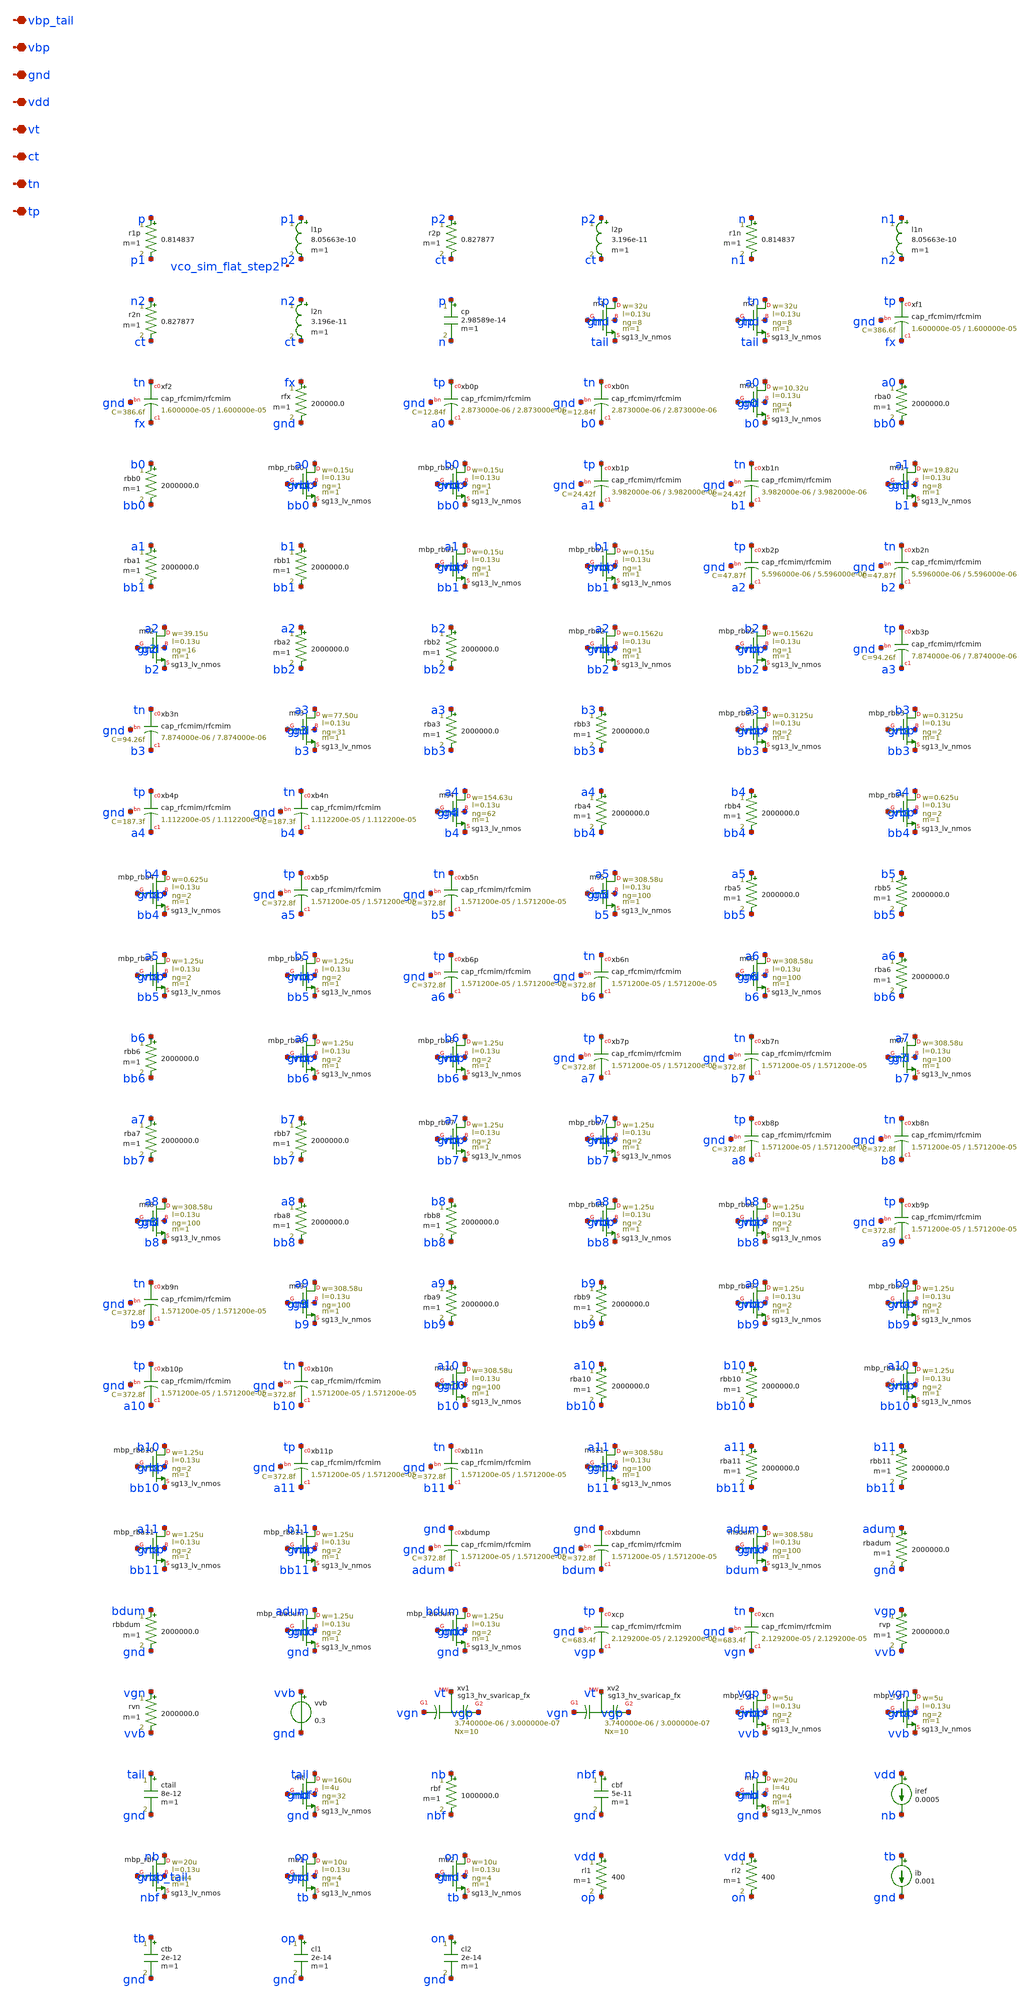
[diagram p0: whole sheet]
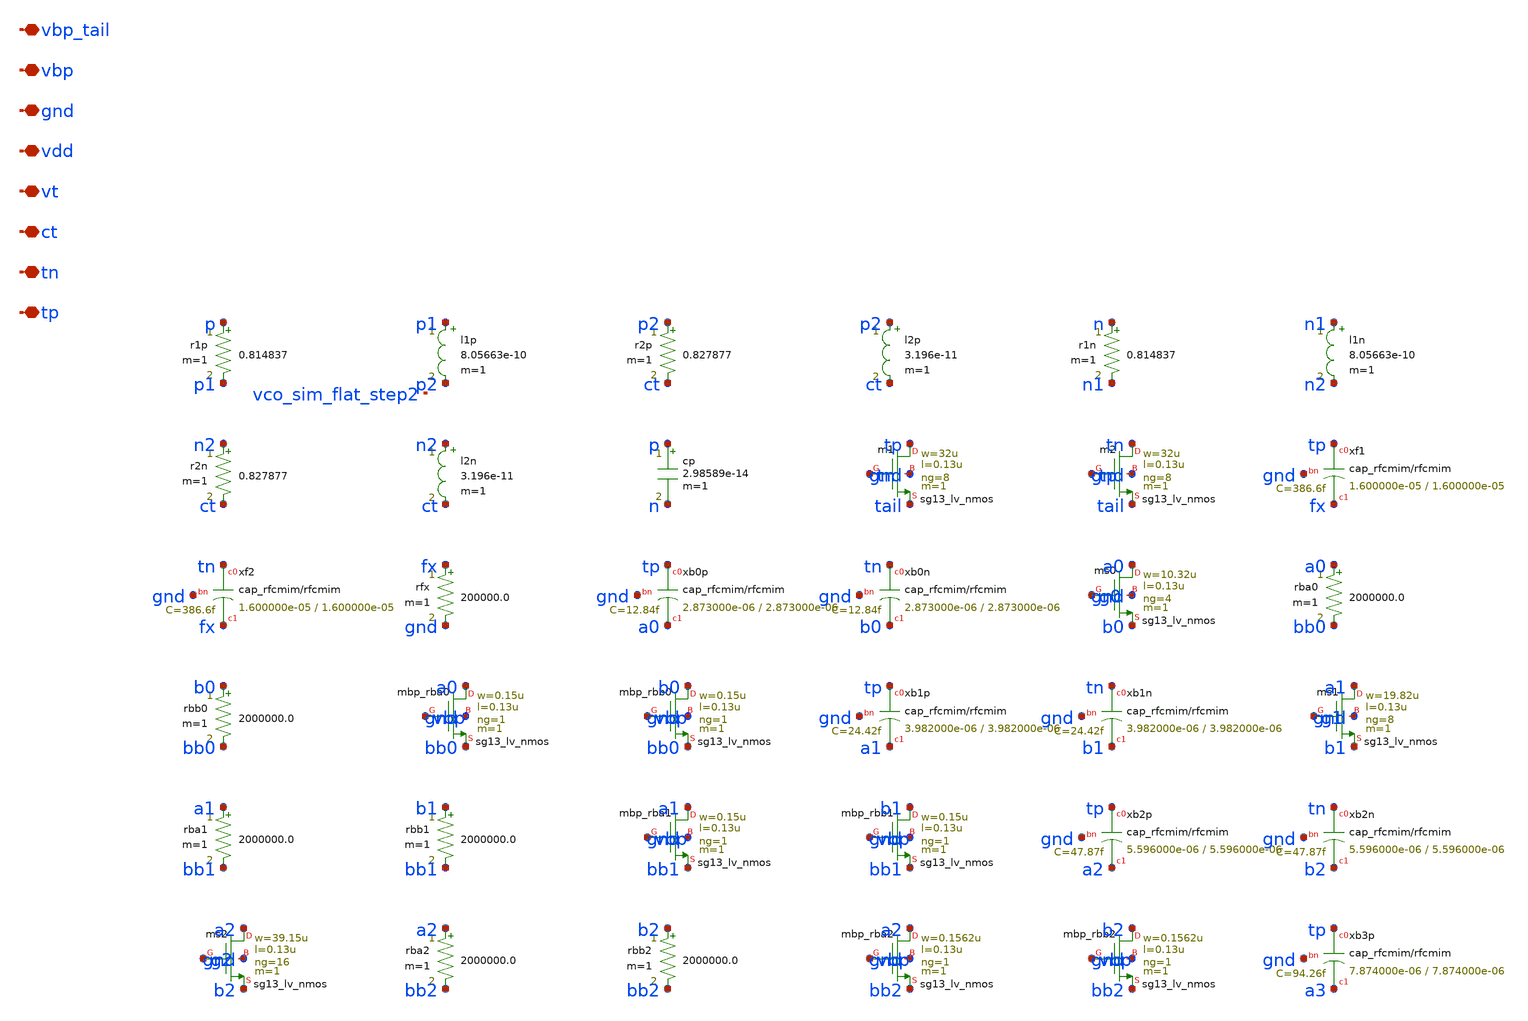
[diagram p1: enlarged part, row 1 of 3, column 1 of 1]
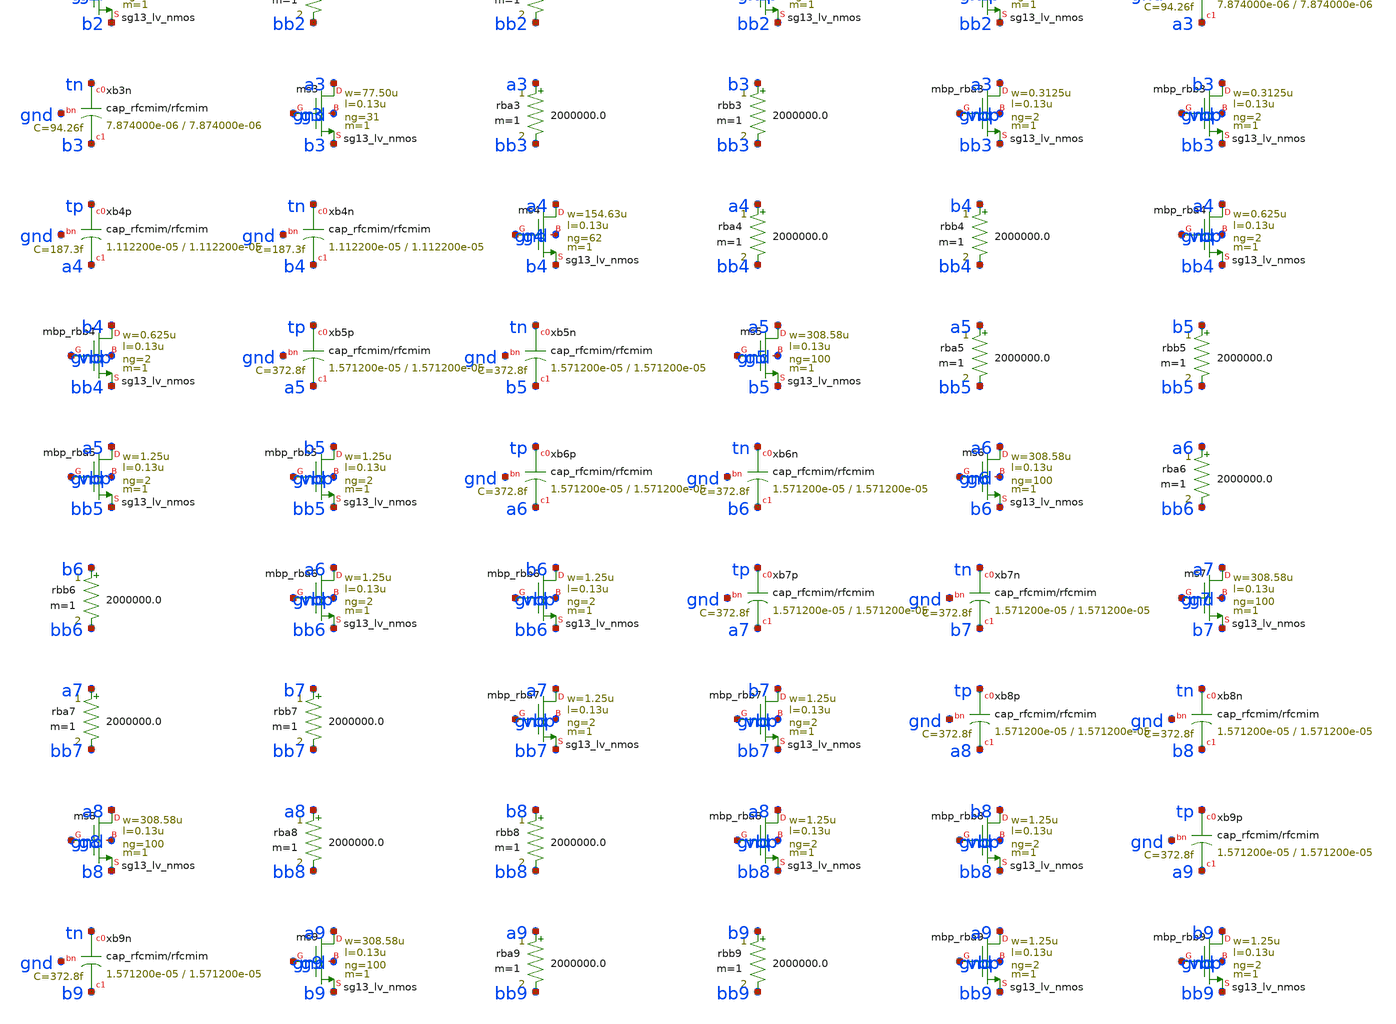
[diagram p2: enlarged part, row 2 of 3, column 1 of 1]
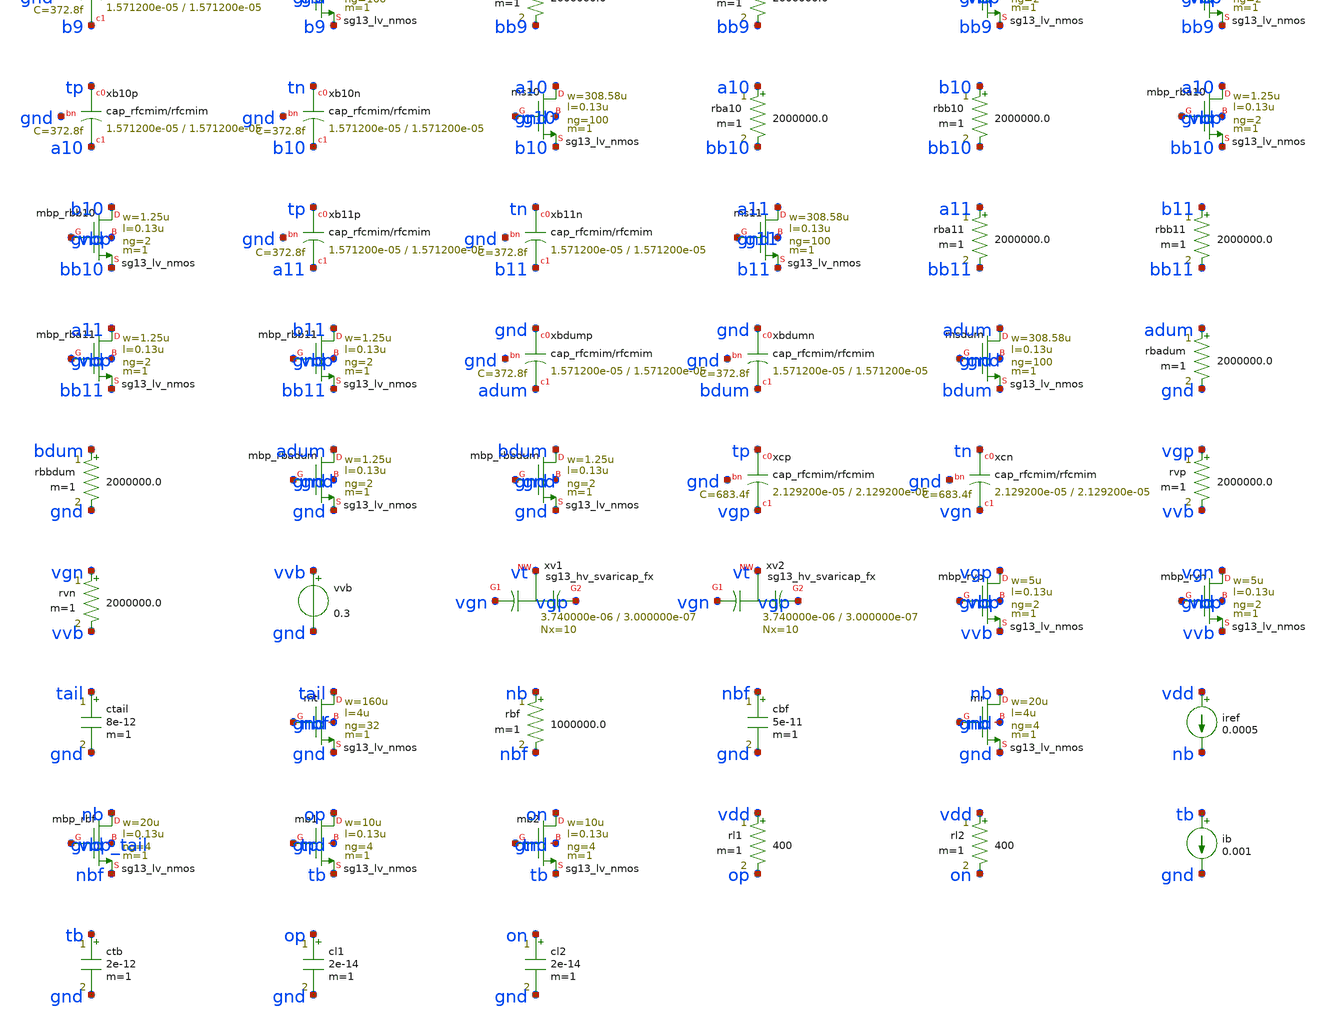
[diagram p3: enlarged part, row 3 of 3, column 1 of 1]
** sch_path: analog/vco/sch/vco_sim_flat.sch
**.subckt vco_sim_flat tp tn ct vt vdd gnd vbp vbp_tail
*.iopin tp
*.iopin tn
*.iopin ct
*.iopin vt
*.iopin vdd
*.iopin gnd
*.iopin vbp
*.iopin vbp_tail
r1p p p1 0.814837 m=1
l1p p1 p2 8.05663e-10 m=1
r2p p2 ct 0.827877 m=1
l2p p2 ct 3.196e-11 m=1
r1n n n1 0.814837 m=1
l1n n1 n2 8.05663e-10 m=1
r2n n2 ct 0.827877 m=1
l2n n2 ct 3.196e-11 m=1
cp p n 2.98589e-14 m=1
Xm1 tp tn tail gnd sg13_lv_nmos w=32u l=0.13u ng=8 m=1 mm_ok=1
Xm2 tn tp tail gnd sg13_lv_nmos w=32u l=0.13u ng=8 m=1 mm_ok=1
Xxf1 tp fx gnd cap_rfcmim w=1.600000e-05 l=1.600000e-05 wfeed=5.0e-6 m=1 mm_ok=1
Xxf2 tn fx gnd cap_rfcmim w=1.600000e-05 l=1.600000e-05 wfeed=5.0e-6 m=1 mm_ok=1
rfx fx gnd 200000.0 m=1
Xxb0p tp a0 gnd cap_rfcmim w=2.873000e-06 l=2.873000e-06 wfeed=5.0e-6 m=1 mm_ok=1
Xxb0n tn b0 gnd cap_rfcmim w=2.873000e-06 l=2.873000e-06 wfeed=5.0e-6 m=1 mm_ok=1
Xms0 a0 g0 b0 gnd sg13_lv_nmos w=10.32u l=0.13u ng=4 m=1 mm_ok=1
rba0 a0 bb0 2000000.0 m=1
rbb0 b0 bb0 2000000.0 m=1
Xmbp_rba0 a0 vbp bb0 gnd sg13_lv_nmos w=0.15u l=0.13u ng=1 m=1 mm_ok=1
Xmbp_rbb0 b0 vbp bb0 gnd sg13_lv_nmos w=0.15u l=0.13u ng=1 m=1 mm_ok=1
Xxb1p tp a1 gnd cap_rfcmim w=3.982000e-06 l=3.982000e-06 wfeed=5.0e-6 m=1 mm_ok=1
Xxb1n tn b1 gnd cap_rfcmim w=3.982000e-06 l=3.982000e-06 wfeed=5.0e-6 m=1 mm_ok=1
Xms1 a1 g1 b1 gnd sg13_lv_nmos w=19.82u l=0.13u ng=8 m=1 mm_ok=1
rba1 a1 bb1 2000000.0 m=1
rbb1 b1 bb1 2000000.0 m=1
Xmbp_rba1 a1 vbp bb1 gnd sg13_lv_nmos w=0.15u l=0.13u ng=1 m=1 mm_ok=1
Xmbp_rbb1 b1 vbp bb1 gnd sg13_lv_nmos w=0.15u l=0.13u ng=1 m=1 mm_ok=1
Xxb2p tp a2 gnd cap_rfcmim w=5.596000e-06 l=5.596000e-06 wfeed=5.0e-6 m=1 mm_ok=1
Xxb2n tn b2 gnd cap_rfcmim w=5.596000e-06 l=5.596000e-06 wfeed=5.0e-6 m=1 mm_ok=1
Xms2 a2 g2 b2 gnd sg13_lv_nmos w=39.15u l=0.13u ng=16 m=1 mm_ok=1
rba2 a2 bb2 2000000.0 m=1
rbb2 b2 bb2 2000000.0 m=1
Xmbp_rba2 a2 vbp bb2 gnd sg13_lv_nmos w=0.1562u l=0.13u ng=1 m=1 mm_ok=1
Xmbp_rbb2 b2 vbp bb2 gnd sg13_lv_nmos w=0.1562u l=0.13u ng=1 m=1 mm_ok=1
Xxb3p tp a3 gnd cap_rfcmim w=7.874000e-06 l=7.874000e-06 wfeed=5.0e-6 m=1 mm_ok=1
Xxb3n tn b3 gnd cap_rfcmim w=7.874000e-06 l=7.874000e-06 wfeed=5.0e-6 m=1 mm_ok=1
Xms3 a3 g3 b3 gnd sg13_lv_nmos w=77.50u l=0.13u ng=31 m=1 mm_ok=1
rba3 a3 bb3 2000000.0 m=1
rbb3 b3 bb3 2000000.0 m=1
Xmbp_rba3 a3 vbp bb3 gnd sg13_lv_nmos w=0.3125u l=0.13u ng=2 m=1 mm_ok=1
Xmbp_rbb3 b3 vbp bb3 gnd sg13_lv_nmos w=0.3125u l=0.13u ng=2 m=1 mm_ok=1
Xxb4p tp a4 gnd cap_rfcmim w=1.112200e-05 l=1.112200e-05 wfeed=5.0e-6 m=1 mm_ok=1
Xxb4n tn b4 gnd cap_rfcmim w=1.112200e-05 l=1.112200e-05 wfeed=5.0e-6 m=1 mm_ok=1
Xms4 a4 g4 b4 gnd sg13_lv_nmos w=154.63u l=0.13u ng=62 m=1 mm_ok=1
rba4 a4 bb4 2000000.0 m=1
rbb4 b4 bb4 2000000.0 m=1
Xmbp_rba4 a4 vbp bb4 gnd sg13_lv_nmos w=0.625u l=0.13u ng=2 m=1 mm_ok=1
Xmbp_rbb4 b4 vbp bb4 gnd sg13_lv_nmos w=0.625u l=0.13u ng=2 m=1 mm_ok=1
Xxb5p tp a5 gnd cap_rfcmim w=1.571200e-05 l=1.571200e-05 wfeed=5.0e-6 m=1 mm_ok=1
Xxb5n tn b5 gnd cap_rfcmim w=1.571200e-05 l=1.571200e-05 wfeed=5.0e-6 m=1 mm_ok=1
Xms5 a5 g5 b5 gnd sg13_lv_nmos w=308.58u l=0.13u ng=100 m=1 mm_ok=1
rba5 a5 bb5 2000000.0 m=1
rbb5 b5 bb5 2000000.0 m=1
Xmbp_rba5 a5 vbp bb5 gnd sg13_lv_nmos w=1.25u l=0.13u ng=2 m=1 mm_ok=1
Xmbp_rbb5 b5 vbp bb5 gnd sg13_lv_nmos w=1.25u l=0.13u ng=2 m=1 mm_ok=1
Xxb6p tp a6 gnd cap_rfcmim w=1.571200e-05 l=1.571200e-05 wfeed=5.0e-6 m=1 mm_ok=1
Xxb6n tn b6 gnd cap_rfcmim w=1.571200e-05 l=1.571200e-05 wfeed=5.0e-6 m=1 mm_ok=1
Xms6 a6 g6 b6 gnd sg13_lv_nmos w=308.58u l=0.13u ng=100 m=1 mm_ok=1
rba6 a6 bb6 2000000.0 m=1
rbb6 b6 bb6 2000000.0 m=1
Xmbp_rba6 a6 vbp bb6 gnd sg13_lv_nmos w=1.25u l=0.13u ng=2 m=1 mm_ok=1
Xmbp_rbb6 b6 vbp bb6 gnd sg13_lv_nmos w=1.25u l=0.13u ng=2 m=1 mm_ok=1
Xxb7p tp a7 gnd cap_rfcmim w=1.571200e-05 l=1.571200e-05 wfeed=5.0e-6 m=1 mm_ok=1
Xxb7n tn b7 gnd cap_rfcmim w=1.571200e-05 l=1.571200e-05 wfeed=5.0e-6 m=1 mm_ok=1
Xms7 a7 g7 b7 gnd sg13_lv_nmos w=308.58u l=0.13u ng=100 m=1 mm_ok=1
rba7 a7 bb7 2000000.0 m=1
rbb7 b7 bb7 2000000.0 m=1
Xmbp_rba7 a7 vbp bb7 gnd sg13_lv_nmos w=1.25u l=0.13u ng=2 m=1 mm_ok=1
Xmbp_rbb7 b7 vbp bb7 gnd sg13_lv_nmos w=1.25u l=0.13u ng=2 m=1 mm_ok=1
Xxb8p tp a8 gnd cap_rfcmim w=1.571200e-05 l=1.571200e-05 wfeed=5.0e-6 m=1 mm_ok=1
Xxb8n tn b8 gnd cap_rfcmim w=1.571200e-05 l=1.571200e-05 wfeed=5.0e-6 m=1 mm_ok=1
Xms8 a8 g8 b8 gnd sg13_lv_nmos w=308.58u l=0.13u ng=100 m=1 mm_ok=1
rba8 a8 bb8 2000000.0 m=1
rbb8 b8 bb8 2000000.0 m=1
Xmbp_rba8 a8 vbp bb8 gnd sg13_lv_nmos w=1.25u l=0.13u ng=2 m=1 mm_ok=1
Xmbp_rbb8 b8 vbp bb8 gnd sg13_lv_nmos w=1.25u l=0.13u ng=2 m=1 mm_ok=1
Xxb9p tp a9 gnd cap_rfcmim w=1.571200e-05 l=1.571200e-05 wfeed=5.0e-6 m=1 mm_ok=1
Xxb9n tn b9 gnd cap_rfcmim w=1.571200e-05 l=1.571200e-05 wfeed=5.0e-6 m=1 mm_ok=1
Xms9 a9 g9 b9 gnd sg13_lv_nmos w=308.58u l=0.13u ng=100 m=1 mm_ok=1
rba9 a9 bb9 2000000.0 m=1
rbb9 b9 bb9 2000000.0 m=1
Xmbp_rba9 a9 vbp bb9 gnd sg13_lv_nmos w=1.25u l=0.13u ng=2 m=1 mm_ok=1
Xmbp_rbb9 b9 vbp bb9 gnd sg13_lv_nmos w=1.25u l=0.13u ng=2 m=1 mm_ok=1
Xxb10p tp a10 gnd cap_rfcmim w=1.571200e-05 l=1.571200e-05 wfeed=5.0e-6 m=1 mm_ok=1
Xxb10n tn b10 gnd cap_rfcmim w=1.571200e-05 l=1.571200e-05 wfeed=5.0e-6 m=1 mm_ok=1
Xms10 a10 g10 b10 gnd sg13_lv_nmos w=308.58u l=0.13u ng=100 m=1 mm_ok=1
rba10 a10 bb10 2000000.0 m=1
rbb10 b10 bb10 2000000.0 m=1
Xmbp_rba10 a10 vbp bb10 gnd sg13_lv_nmos w=1.25u l=0.13u ng=2 m=1 mm_ok=1
Xmbp_rbb10 b10 vbp bb10 gnd sg13_lv_nmos w=1.25u l=0.13u ng=2 m=1 mm_ok=1
Xxb11p tp a11 gnd cap_rfcmim w=1.571200e-05 l=1.571200e-05 wfeed=5.0e-6 m=1 mm_ok=1
Xxb11n tn b11 gnd cap_rfcmim w=1.571200e-05 l=1.571200e-05 wfeed=5.0e-6 m=1 mm_ok=1
Xms11 a11 g11 b11 gnd sg13_lv_nmos w=308.58u l=0.13u ng=100 m=1 mm_ok=1
rba11 a11 bb11 2000000.0 m=1
rbb11 b11 bb11 2000000.0 m=1
Xmbp_rba11 a11 vbp bb11 gnd sg13_lv_nmos w=1.25u l=0.13u ng=2 m=1 mm_ok=1
Xmbp_rbb11 b11 vbp bb11 gnd sg13_lv_nmos w=1.25u l=0.13u ng=2 m=1 mm_ok=1
Xxbdump gnd adum gnd cap_rfcmim w=1.571200e-05 l=1.571200e-05 wfeed=5.0e-6 m=1 mm_ok=1
Xxbdumn gnd bdum gnd cap_rfcmim w=1.571200e-05 l=1.571200e-05 wfeed=5.0e-6 m=1 mm_ok=1
Xmsdum adum gnd bdum gnd sg13_lv_nmos w=308.58u l=0.13u ng=100 m=1 mm_ok=1
rbadum adum gnd 2000000.0 m=1
rbbdum bdum gnd 2000000.0 m=1
Xmbp_rbadum adum gnd gnd gnd sg13_lv_nmos w=1.25u l=0.13u ng=2 m=1 mm_ok=1
Xmbp_rbbdum bdum gnd gnd gnd sg13_lv_nmos w=1.25u l=0.13u ng=2 m=1 mm_ok=1
Xxcp tp vgp gnd cap_rfcmim w=2.129200e-05 l=2.129200e-05 wfeed=5.0e-6 m=1 mm_ok=1
Xxcn tn vgn gnd cap_rfcmim w=2.129200e-05 l=2.129200e-05 wfeed=5.0e-6 m=1 mm_ok=1
rvp vgp vvb 2000000.0 m=1
rvn vgn vvb 2000000.0 m=1
vvb vvb gnd 0.3
Xxv1 vgn vt vgp sub! sg13_hv_svaricap_fx w=3.740000e-06 l=3.000000e-07 Nx=10 mm_ok=1
Xxv2 vgn vt vgp sub! sg13_hv_svaricap_fx w=3.740000e-06 l=3.000000e-07 Nx=10 mm_ok=1
Xmbp_rvp vgp vbp vvb gnd sg13_lv_nmos w=5u l=0.13u ng=2 m=1 mm_ok=1
Xmbp_rvn vgn vbp vvb gnd sg13_lv_nmos w=5u l=0.13u ng=2 m=1 mm_ok=1
ctail tail gnd 8e-12 m=1
Xmt tail nbf gnd gnd sg13_lv_nmos w=160u l=4u ng=32 m=1 mm_ok=1
rbf nb nbf 1000000.0 m=1
cbf nbf gnd 5e-11 m=1
Xmr nb nb gnd gnd sg13_lv_nmos w=20u l=4u ng=4 m=1 mm_ok=1
iref vdd nb 0.0005
Xmbp_rbf nb vbp_tail nbf gnd sg13_lv_nmos w=20u l=0.13u ng=4 m=1 mm_ok=1
Xmb1 op tp tb gnd sg13_lv_nmos w=10u l=0.13u ng=4 m=1 mm_ok=1
Xmb2 on tn tb gnd sg13_lv_nmos w=10u l=0.13u ng=4 m=1 mm_ok=1
rl1 vdd op 400 m=1
rl2 vdd on 400 m=1
ib tb gnd 0.001
ctb tb gnd 2e-12 m=1
cl1 op gnd 2e-14 m=1
cl2 on gnd 2e-14 m=1
**.ends
.end
